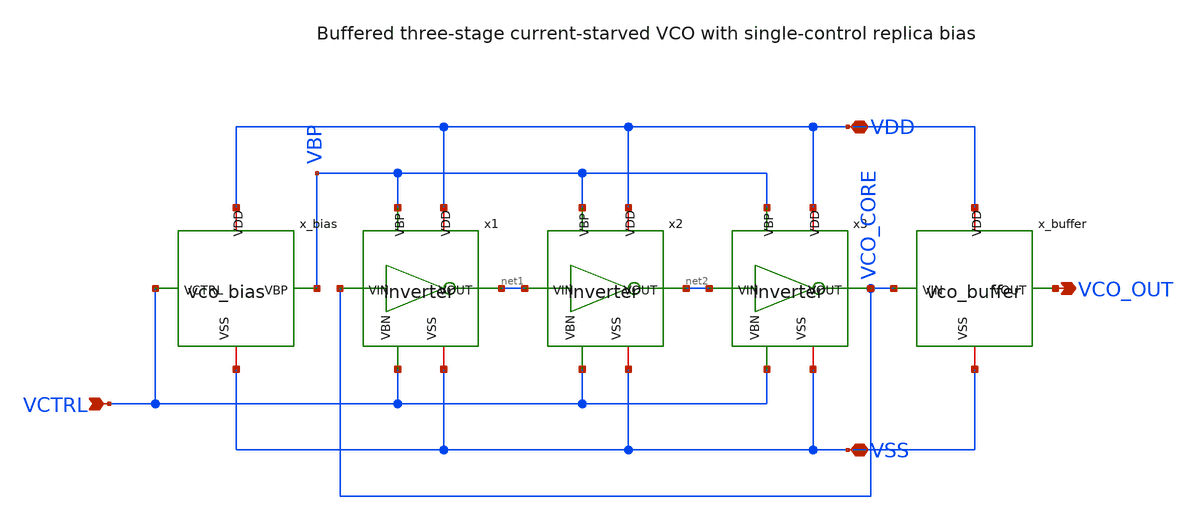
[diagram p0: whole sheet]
** sch_path: macros/pll_analog/schematic/xschem/ring_oscillator.sch
**.subckt ring_oscillator VCTRL VDD VSS VCO_OUT
*.ipin VCTRL
*.iopin VDD
*.iopin VSS
*.opin VCO_OUT
x1 VCO_CORE net1 VBP VDD VCTRL VSS inverter
x2 net1 net2 VBP VDD VCTRL VSS inverter
x3 net2 VCO_CORE VBP VDD VCTRL VSS inverter
x_bias VCTRL VBP VDD VSS vco_bias
x_buffer VCO_CORE VCO_OUT VDD VSS vco_buffer
**.ends
.end
